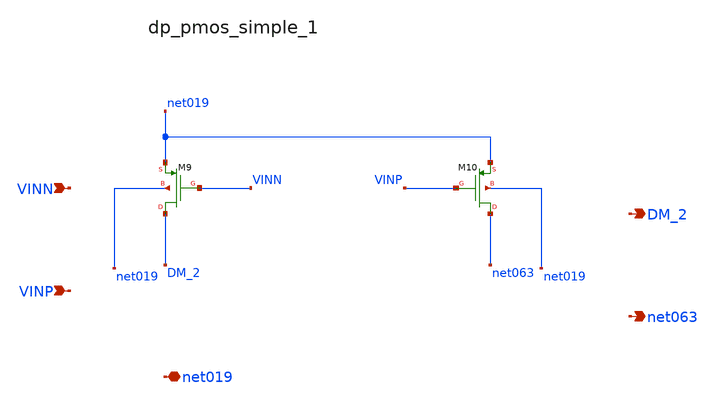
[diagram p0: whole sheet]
** sch_path: analog-db/raw/amp_013_qu2017_azc/hier/blocks/dp_pmos_simple_1.sch
**.subckt dp_pmos_simple_1 VINN VINP net019 DM_2 net063
*.ipin VINN
*.ipin VINP
*.iopin net019
*.opin DM_2
*.opin net063
XM10 net063 VINP net019 net019 sg13_lv_pmos w=x_dut_xm10_w l=x_dut_xm10_l ng=1 m=x_dut_xm10_m
XM9 DM_2 VINN net019 net019 sg13_lv_pmos w=x_dut_xm9_w l=x_dut_xm9_l ng=1 m=x_dut_xm9_m
**.ends
.end
